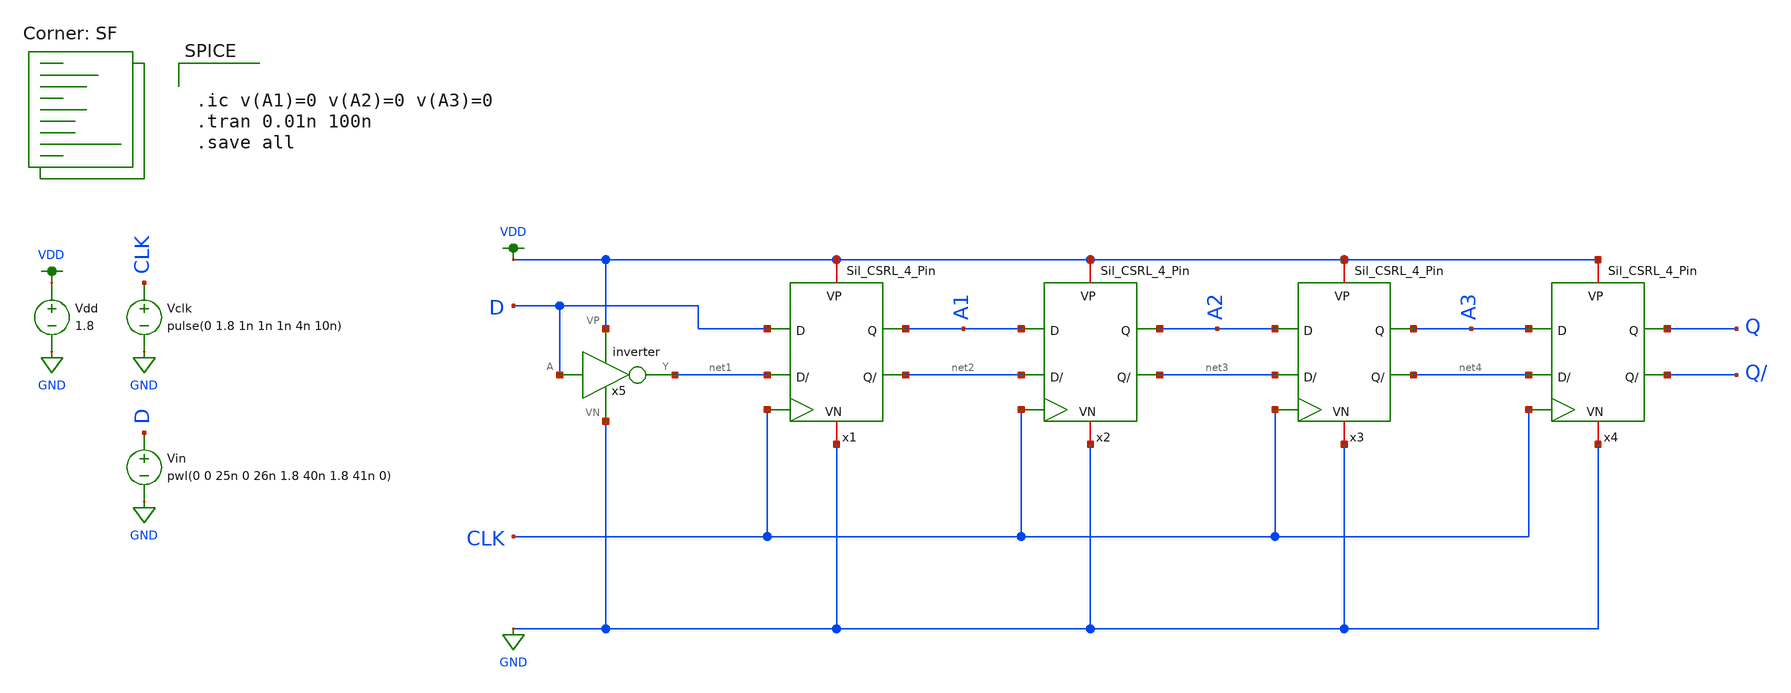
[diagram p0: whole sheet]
** sch_path: MADVLSI_MP2/Shift_Reg_V1.sch
**.subckt Shift_Reg_V1
x5 VDD D net1 GND inverter
Vdd VDD GND 1.8
Vclk CLK GND pulse(0 1.8 1n 1n 1n 4n 10n)
Vin D GND pwl(0 0 25n 0 26n 1.8 40n 1.8 41n 0)
x1 VDD D A1 net2 net1 CLK GND Sil_CSRL_4_Pin
x2 VDD A1 A2 net3 net2 CLK GND Sil_CSRL_4_Pin
x3 VDD A2 A3 net4 net3 CLK GND Sil_CSRL_4_Pin
x4 VDD A3 Q Q/ net4 CLK GND Sil_CSRL_4_Pin
**** begin user architecture code


.ic v(A1)=0 v(A2)=0 v(A3)=0
.tran 0.01n 100n
.save all

.lib $::SKYWATER_MODELS/sky130.lib.spice SF
**** end user architecture code
**.ends

* expanding   symbol:  /home/allan/Documents/MADVLSI_Projects/MADVLSI_MP1/inverter.sym # of pins=4
** sym_path: MADVLSI_MP1/inverter.sym
** sch_path: MADVLSI_MP1/inverter.sch
.subckt inverter VP A Y VN
*.ipin A
*.iopin VP
*.iopin VN
*.opin Y
XM1 Y A VN VN sky130_fd_pr__nfet_01v8 L=0.15 W=1 nf=1 ad='int((nf+1)/2) * W/nf * 0.29' as='int((nf+2)/2) * W/nf * 0.29'
+ pd='2*int((nf+1)/2) * (W/nf + 0.29)' ps='2*int((nf+2)/2) * (W/nf + 0.29)' nrd='0.29 / W' nrs='0.29 / W'
+ sa=0 sb=0 sd=0 mult=1 m=1
XM2 Y A VP VP sky130_fd_pr__pfet_01v8 L=0.15 W=1 nf=1 ad='int((nf+1)/2) * W/nf * 0.29' as='int((nf+2)/2) * W/nf * 0.29'
+ pd='2*int((nf+1)/2) * (W/nf + 0.29)' ps='2*int((nf+2)/2) * (W/nf + 0.29)' nrd='0.29 / W' nrs='0.29 / W'
+ sa=0 sb=0 sd=0 mult=1 m=1
.ends


* expanding   symbol:  Sil_CSRL_4_Pin.sym # of pins=7
** sym_path: MADVLSI_MP2/Sil_CSRL_4_Pin.sym
** sch_path: MADVLSI_MP2/Sil_CSRL_4_Pin.sch
.subckt Sil_CSRL_4_Pin VP D Q QBar DBar clk VN
*.iopin VN
*.iopin VP
*.ipin D
*.ipin DBar
*.ipin clk
*.opin Q
*.opin QBar
XQ1 net1 clk D VP sky130_fd_pr__pfet_01v8 L=0.15 W=0.9 nf=1 ad='int((nf+1)/2) * W/nf * 0.29' as='int((nf+2)/2) * W/nf * 0.29'
+ pd='2*int((nf+1)/2) * (W/nf + 0.29)' ps='2*int((nf+2)/2) * (W/nf + 0.29)' nrd='0.29 / W' nrs='0.29 / W'
+ sa=0 sb=0 sd=0 mult=1 m=1
XQ3 Q clk net1 VN sky130_fd_pr__nfet_01v8 L=0.15 W=0.9 nf=1 ad='int((nf+1)/2) * W/nf * 0.29' as='int((nf+2)/2) * W/nf * 0.29'
+ pd='2*int((nf+1)/2) * (W/nf + 0.29)' ps='2*int((nf+2)/2) * (W/nf + 0.29)' nrd='0.29 / W' nrs='0.29 / W'
+ sa=0 sb=0 sd=0 mult=1 m=1
XQ2 net2 clk DBar VP sky130_fd_pr__pfet_01v8 L=0.15 W=0.9 nf=1 ad='int((nf+1)/2) * W/nf * 0.29' as='int((nf+2)/2) * W/nf * 0.29'
+ pd='2*int((nf+1)/2) * (W/nf + 0.29)' ps='2*int((nf+2)/2) * (W/nf + 0.29)' nrd='0.29 / W' nrs='0.29 / W'
+ sa=0 sb=0 sd=0 mult=1 m=1
XQ8 net2 net1 VP VP sky130_fd_pr__pfet_01v8 L=0.15 W=0.9 nf=1 ad='int((nf+1)/2) * W/nf * 0.29' as='int((nf+2)/2) * W/nf * 0.29'
+ pd='2*int((nf+1)/2) * (W/nf + 0.29)' ps='2*int((nf+2)/2) * (W/nf + 0.29)' nrd='0.29 / W' nrs='0.29 / W'
+ sa=0 sb=0 sd=0 mult=1 m=1
XQ9 VP net2 net1 VP sky130_fd_pr__pfet_01v8 L=0.15 W=0.9 nf=1 ad='int((nf+1)/2) * W/nf * 0.29' as='int((nf+2)/2) * W/nf * 0.29'
+ pd='2*int((nf+1)/2) * (W/nf + 0.29)' ps='2*int((nf+2)/2) * (W/nf + 0.29)' nrd='0.29 / W' nrs='0.29 / W'
+ sa=0 sb=0 sd=0 mult=1 m=1
XQ12 net4 QBar Q VP sky130_fd_pr__pfet_01v8 L=0.15 W=0.9 nf=1 ad='int((nf+1)/2) * W/nf * 0.29' as='int((nf+2)/2) * W/nf * 0.29'
+ pd='2*int((nf+1)/2) * (W/nf + 0.29)' ps='2*int((nf+2)/2) * (W/nf + 0.29)' nrd='0.29 / W' nrs='0.29 / W'
+ sa=0 sb=0 sd=0 mult=1 m=1
XQ10 net4 clk VP VP sky130_fd_pr__pfet_01v8 L=0.15 W=0.9 nf=1 ad='int((nf+1)/2) * W/nf * 0.29' as='int((nf+2)/2) * W/nf * 0.29'
+ pd='2*int((nf+1)/2) * (W/nf + 0.29)' ps='2*int((nf+2)/2) * (W/nf + 0.29)' nrd='0.29 / W' nrs='0.29 / W'
+ sa=0 sb=0 sd=0 mult=1 m=1
XQ11 QBar Q net4 VP sky130_fd_pr__pfet_01v8 L=0.15 W=0.9 nf=1 ad='int((nf+1)/2) * W/nf * 0.29' as='int((nf+2)/2) * W/nf * 0.29'
+ pd='2*int((nf+1)/2) * (W/nf + 0.29)' ps='2*int((nf+2)/2) * (W/nf + 0.29)' nrd='0.29 / W' nrs='0.29 / W'
+ sa=0 sb=0 sd=0 mult=1 m=1
XQ4 QBar clk net2 VN sky130_fd_pr__nfet_01v8 L=0.15 W=0.9 nf=1 ad='int((nf+1)/2) * W/nf * 0.29' as='int((nf+2)/2) * W/nf * 0.29'
+ pd='2*int((nf+1)/2) * (W/nf + 0.29)' ps='2*int((nf+2)/2) * (W/nf + 0.29)' nrd='0.29 / W' nrs='0.29 / W'
+ sa=0 sb=0 sd=0 mult=1 m=1
XQ5a net3 clk VN VN sky130_fd_pr__nfet_01v8 L=0.15 W=0.45 nf=1 ad='int((nf+1)/2) * W/nf * 0.29' as='int((nf+2)/2) * W/nf * 0.29'
+ pd='2*int((nf+1)/2) * (W/nf + 0.29)' ps='2*int((nf+2)/2) * (W/nf + 0.29)' nrd='0.29 / W' nrs='0.29 / W'
+ sa=0 sb=0 sd=0 mult=1 m=1
XQ7 net3 net2 net1 VN sky130_fd_pr__nfet_01v8 L=0.15 W=0.45 nf=1 ad='int((nf+1)/2) * W/nf * 0.29' as='int((nf+2)/2) * W/nf * 0.29'
+ pd='2*int((nf+1)/2) * (W/nf + 0.29)' ps='2*int((nf+2)/2) * (W/nf + 0.29)' nrd='0.29 / W' nrs='0.29 / W'
+ sa=0 sb=0 sd=0 mult=1 m=1
XQ6 net2 net1 net3 VN sky130_fd_pr__nfet_01v8 L=0.15 W=0.45 nf=1 ad='int((nf+1)/2) * W/nf * 0.29' as='int((nf+2)/2) * W/nf * 0.29'
+ pd='2*int((nf+1)/2) * (W/nf + 0.29)' ps='2*int((nf+2)/2) * (W/nf + 0.29)' nrd='0.29 / W' nrs='0.29 / W'
+ sa=0 sb=0 sd=0 mult=1 m=1
XQ13 QBar Q VN VN sky130_fd_pr__nfet_01v8 L=0.15 W=0.45 nf=1 ad='int((nf+1)/2) * W/nf * 0.29' as='int((nf+2)/2) * W/nf * 0.29'
+ pd='2*int((nf+1)/2) * (W/nf + 0.29)' ps='2*int((nf+2)/2) * (W/nf + 0.29)' nrd='0.29 / W' nrs='0.29 / W'
+ sa=0 sb=0 sd=0 mult=1 m=1
XQ14 VN QBar Q VN sky130_fd_pr__nfet_01v8 L=0.15 W=0.45 nf=1 ad='int((nf+1)/2) * W/nf * 0.29' as='int((nf+2)/2) * W/nf * 0.29'
+ pd='2*int((nf+1)/2) * (W/nf + 0.29)' ps='2*int((nf+2)/2) * (W/nf + 0.29)' nrd='0.29 / W' nrs='0.29 / W'
+ sa=0 sb=0 sd=0 mult=1 m=1
XQ5b VN clk net3 VN sky130_fd_pr__nfet_01v8 L=0.15 W=0.45 nf=1 ad='int((nf+1)/2) * W/nf * 0.29' as='int((nf+2)/2) * W/nf * 0.29'
+ pd='2*int((nf+1)/2) * (W/nf + 0.29)' ps='2*int((nf+2)/2) * (W/nf + 0.29)' nrd='0.29 / W' nrs='0.29 / W'
+ sa=0 sb=0 sd=0 mult=1 m=1
XQ10b VP clk net4 VP sky130_fd_pr__pfet_01v8 L=0.15 W=0.9 nf=1 ad='int((nf+1)/2) * W/nf * 0.29' as='int((nf+2)/2) * W/nf * 0.29'
+ pd='2*int((nf+1)/2) * (W/nf + 0.29)' ps='2*int((nf+2)/2) * (W/nf + 0.29)' nrd='0.29 / W' nrs='0.29 / W'
+ sa=0 sb=0 sd=0 mult=1 m=1
.ends

.GLOBAL GND
.GLOBAL VDD
.end
